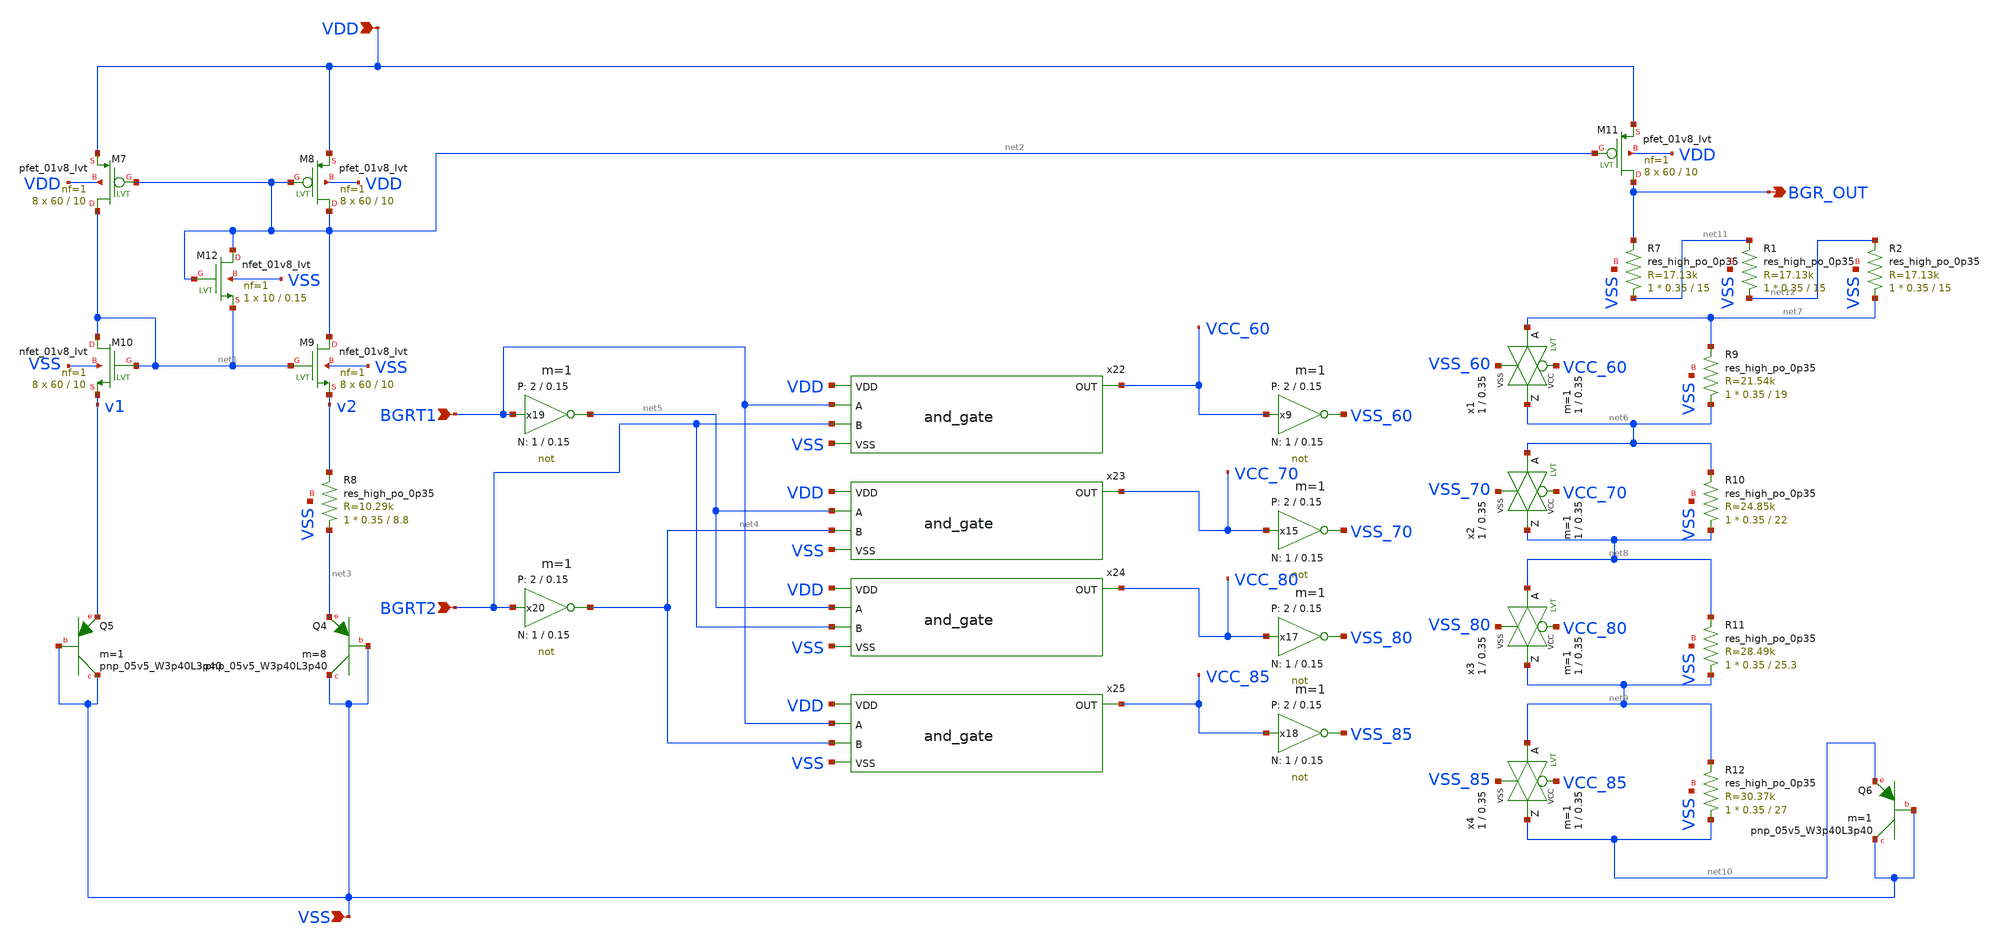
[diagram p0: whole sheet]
** sch_path: xschem/bandgap.sch
**.subckt bandgap BGR_OUT VDD VSS BGRT1 BGRT2
*.opin BGR_OUT
*.ipin VDD
*.ipin VSS
*.ipin BGRT1
*.ipin BGRT2
XM7 net1 net2 VDD VDD sky130_fd_pr__pfet_01v8_lvt L=10 W=60 nf=1 ad='int((nf+1)/2) * W/nf * 0.29' as='int((nf+2)/2) * W/nf * 0.29'
+ pd='2*int((nf+1)/2) * (W/nf + 0.29)' ps='2*int((nf+2)/2) * (W/nf + 0.29)' nrd='0.29 / W' nrs='0.29 / W'
+ sa=0 sb=0 sd=0 mult=8 m=8
XM8 net2 net2 VDD VDD sky130_fd_pr__pfet_01v8_lvt L=10 W=60 nf=1 ad='int((nf+1)/2) * W/nf * 0.29' as='int((nf+2)/2) * W/nf * 0.29'
+ pd='2*int((nf+1)/2) * (W/nf + 0.29)' ps='2*int((nf+2)/2) * (W/nf + 0.29)' nrd='0.29 / W' nrs='0.29 / W'
+ sa=0 sb=0 sd=0 mult=8 m=8
XM9 net2 net1 v2 VSS sky130_fd_pr__nfet_01v8_lvt L=10 W=60 nf=1 ad='int((nf+1)/2) * W/nf * 0.29' as='int((nf+2)/2) * W/nf * 0.29'
+ pd='2*int((nf+1)/2) * (W/nf + 0.29)' ps='2*int((nf+2)/2) * (W/nf + 0.29)' nrd='0.29 / W' nrs='0.29 / W'
+ sa=0 sb=0 sd=0 mult=8 m=8
XM10 net1 net1 v1 VSS sky130_fd_pr__nfet_01v8_lvt L=10 W=60 nf=1 ad='int((nf+1)/2) * W/nf * 0.29' as='int((nf+2)/2) * W/nf * 0.29'
+ pd='2*int((nf+1)/2) * (W/nf + 0.29)' ps='2*int((nf+2)/2) * (W/nf + 0.29)' nrd='0.29 / W' nrs='0.29 / W'
+ sa=0 sb=0 sd=0 mult=8 m=8
XQ4 VSS VSS net3 sky130_fd_pr__pnp_05v5_W3p40L3p40 m=8
XQ5 VSS VSS v1 sky130_fd_pr__pnp_05v5_W3p40L3p40 m=1
XM11 BGR_OUT net2 VDD VDD sky130_fd_pr__pfet_01v8_lvt L=10 W=60 nf=1 ad='int((nf+1)/2) * W/nf * 0.29'
+ as='int((nf+2)/2) * W/nf * 0.29' pd='2*int((nf+1)/2) * (W/nf + 0.29)' ps='2*int((nf+2)/2) * (W/nf + 0.29)'
+ nrd='0.29 / W' nrs='0.29 / W' sa=0 sb=0 sd=0 mult=8 m=8
x9 VSS_60 VCC_60 VCC VSS not W_N=1 L_N=0.15 W_P=2 L_P=0.15 m=1
x15 VSS_70 VCC_70 VCC VSS not W_N=1 L_N=0.15 W_P=2 L_P=0.15 m=1
x17 VSS_80 VCC_80 VCC VSS not W_N=1 L_N=0.15 W_P=2 L_P=0.15 m=1
x18 VSS_85 VCC_85 VCC VSS not W_N=1 L_N=0.15 W_P=2 L_P=0.15 m=1
x19 net5 BGRT1 VCC VSS not W_N=1 L_N=0.15 W_P=2 L_P=0.15 m=1
x20 net4 BGRT2 VCC VSS not W_N=1 L_N=0.15 W_P=2 L_P=0.15 m=1
XR7 net11 BGR_OUT VSS sky130_fd_pr__res_high_po_0p35 L=15 mult=1 m=1
XM12 net2 net2 net1 VSS sky130_fd_pr__nfet_01v8_lvt L=0.15 W=10 nf=1 ad='int((nf+1)/2) * W/nf * 0.29'
+ as='int((nf+2)/2) * W/nf * 0.29' pd='2*int((nf+1)/2) * (W/nf + 0.29)' ps='2*int((nf+2)/2) * (W/nf + 0.29)'
+ nrd='0.29 / W' nrs='0.29 / W' sa=0 sb=0 sd=0 mult=1 m=1
XR8 net3 v2 VSS sky130_fd_pr__res_high_po_0p35 L=8.8 mult=1 m=1
XR9 net6 net7 VSS sky130_fd_pr__res_high_po_0p35 L=19 mult=1 m=1
x22 VDD BGRT1 VCC_60 BGRT2 VSS and_gate
x23 VDD net5 VCC_70 net4 VSS and_gate
x24 VDD net5 VCC_80 BGRT2 VSS and_gate
x25 VDD BGRT1 VCC_85 net4 VSS and_gate
XR10 net8 net6 VSS sky130_fd_pr__res_high_po_0p35 L=22 mult=1 m=1
XR11 net9 net8 VSS sky130_fd_pr__res_high_po_0p35 L=25.3 mult=1 m=1
XR12 net10 net9 VSS sky130_fd_pr__res_high_po_0p35 L=27 mult=1 m=1
XQ6 VSS VSS net10 sky130_fd_pr__pnp_05v5_W3p40L3p40 m=1
x1 net6 net7 VCC_60 VSS_60 VCC VSS passgate_nlvt W_N=1 L_N=0.35 W_P=1 L_P=0.35 m=1
x2 net8 net6 VCC_70 VSS_70 VCC VSS passgate_nlvt W_N=1 L_N=0.35 W_P=1 L_P=0.35 m=1
x3 net9 net8 VCC_80 VSS_80 VCC VSS passgate_nlvt W_N=1 L_N=0.35 W_P=1 L_P=0.35 m=1
x4 net10 net9 VCC_85 VSS_85 VCC VSS passgate_nlvt W_N=1 L_N=0.35 W_P=1 L_P=0.35 m=1
XR1 net12 net11 VSS sky130_fd_pr__res_high_po_0p35 L=15 mult=1 m=1
XR2 net7 net12 VSS sky130_fd_pr__res_high_po_0p35 L=15 mult=1 m=1
**.ends
.end
